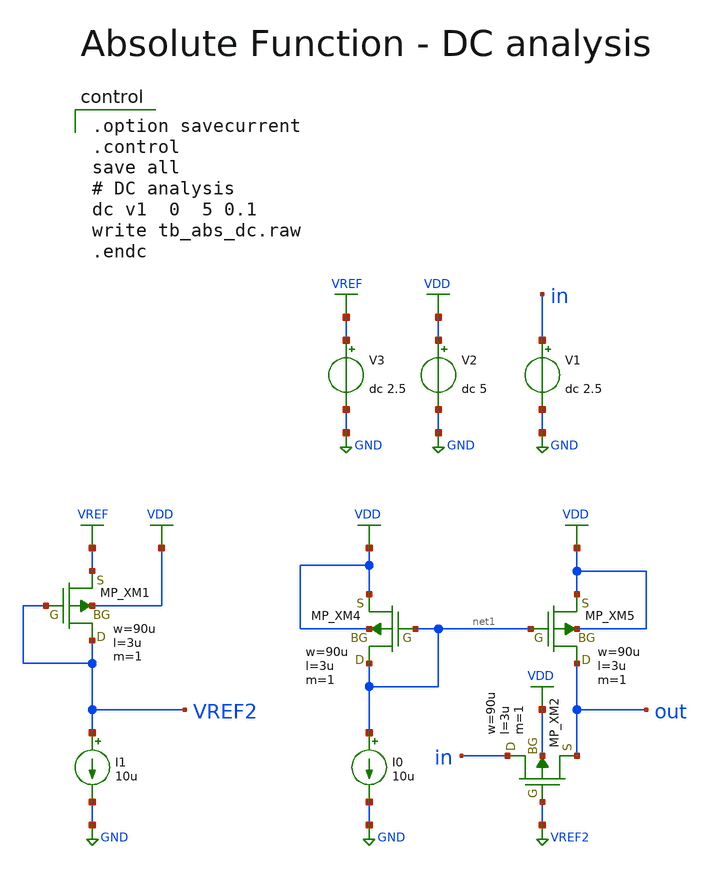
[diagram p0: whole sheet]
** sch_path: member_project/AM_Radio/Yamada3/xschem/tb_abs_dc.sch
**.subckt tb_abs_dc
V2 VDD GND dc 5
I0 net1 GND 10u
V3 VREF GND dc 2.5
XM4 net1 net1 VDD VDD PMOS w=90u l=3u as=0 ad=0 ps=0 pd=0 nrd=0 nrs=0 m=1
XM5 out net1 VDD VDD PMOS w=90u l=3u as=0 ad=0 ps=0 pd=0 nrd=0 nrs=0 m=1
XM2 in VREF2 out VDD PMOS w=90u l=3u as=0 ad=0 ps=0 pd=0 nrd=0 nrs=0 m=1
I1 VREF2 GND 10u
XM1 VREF2 VREF2 VREF VDD PMOS w=90u l=3u as=0 ad=0 ps=0 pd=0 nrd=0 nrs=0 m=1
V1 in GND dc 2.5
**** begin user architecture code

.option savecurrent
.control
save all
# DC analysis
dc v1  0  5 0.1
write tb_abs_dc.raw
.endc

 .include $::LIB/../ip62_models
**** end user architecture code
**.ends
.GLOBAL GND
.GLOBAL VDD
.GLOBAL VREF
.GLOBAL VREF2
.end
